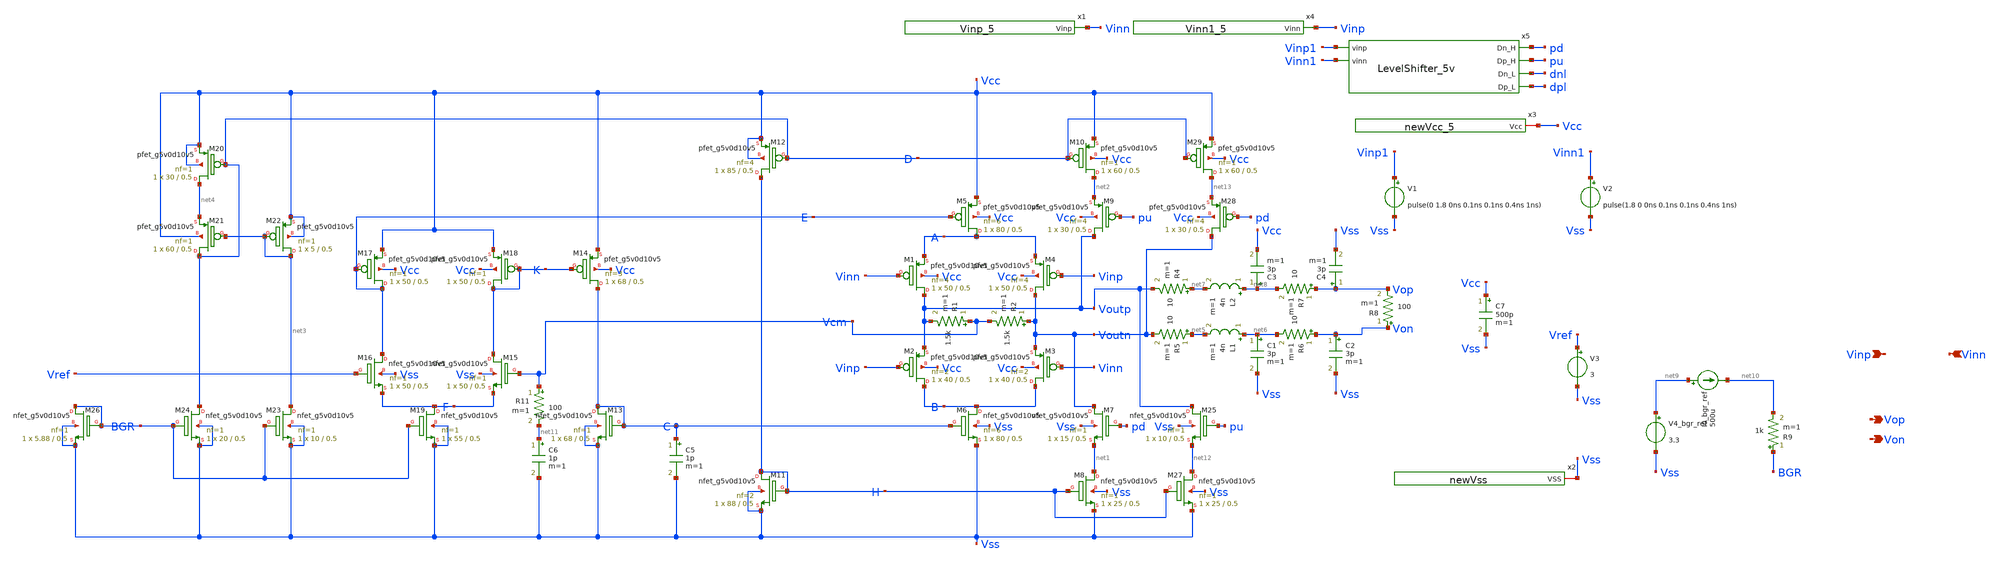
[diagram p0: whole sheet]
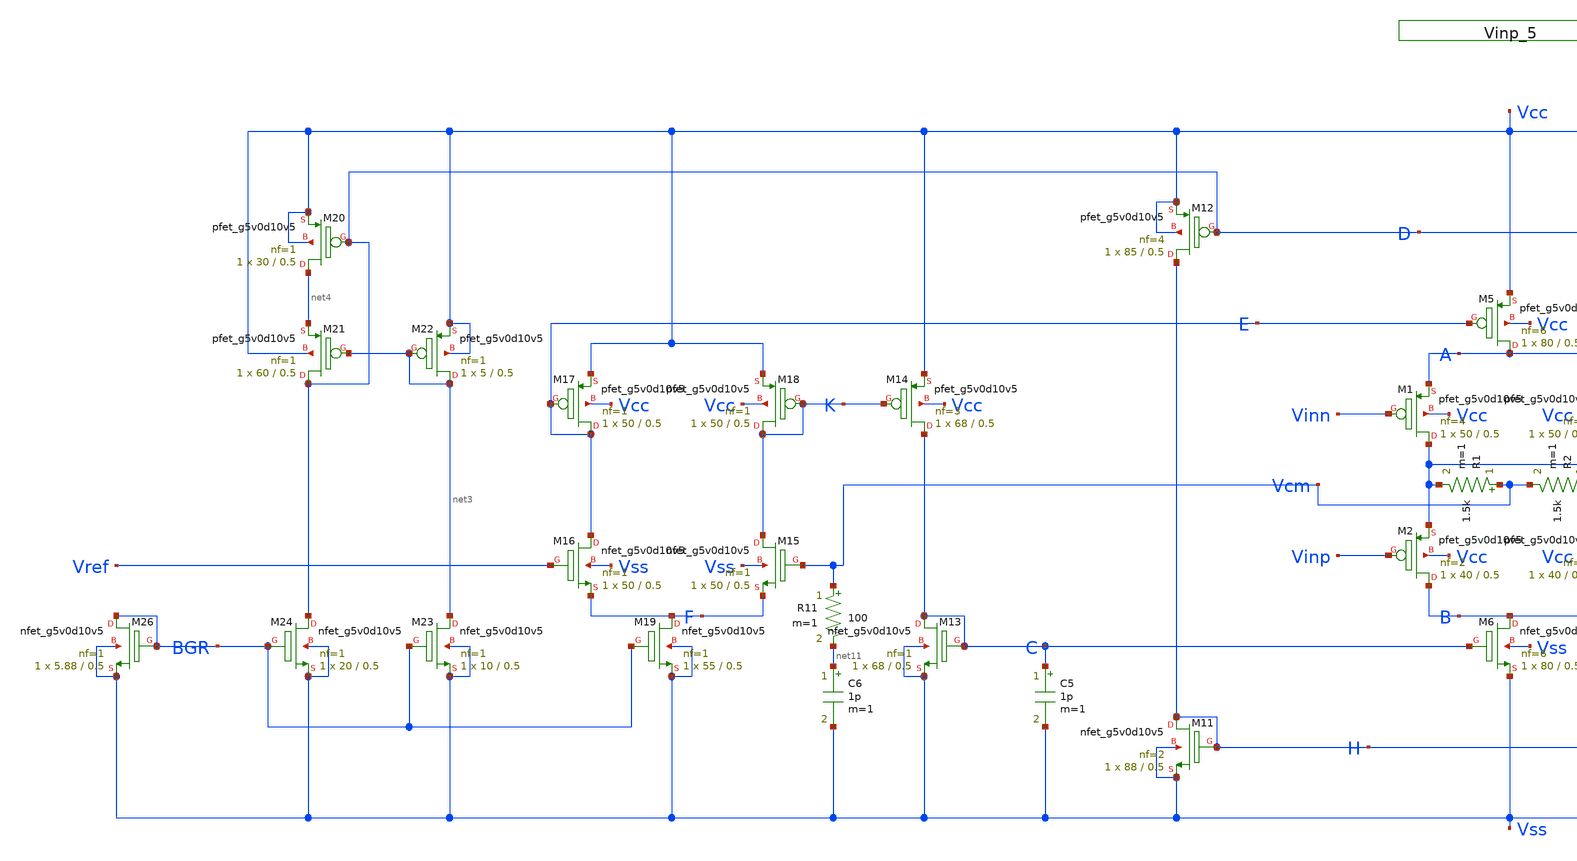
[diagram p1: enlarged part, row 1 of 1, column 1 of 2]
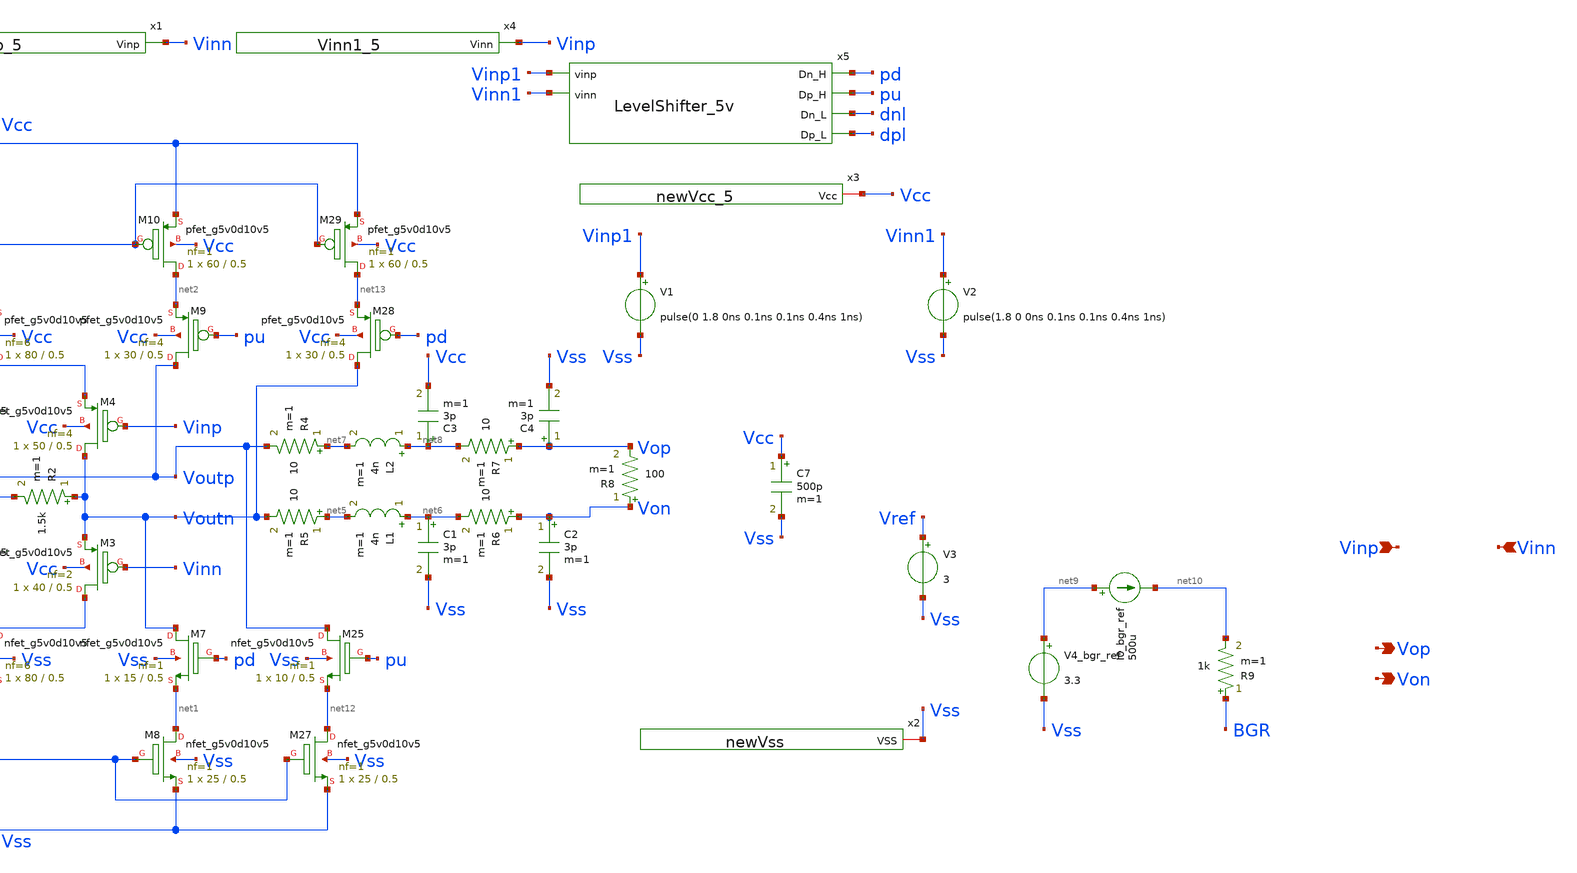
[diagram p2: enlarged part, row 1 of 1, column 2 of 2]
** sch_path: Git Files/Simulation Schematic/OutputDriverOffice_5v_sym.sch
**.subckt OutputDriverOffice_5v_sym Vinp Vinn Vop Von
*.ipin Vinp
*.ipin Vinn
*.opin Vop
*.opin Von
x2 Vss newVss
R1 Vcm Voutp 1.5k m=1
R2 Voutn Vcm 1.5k m=1
V3 Vref Vss 3
I0_bgr_ref net9 net10 500u
R4 net7 Voutp 10 m=1
R5 net5 Voutn 10 m=1
C1 net6 Vss 3p m=1
R6 Von net6 10 m=1
C2 Von Vss 3p m=1
C3 net8 Vcc 3p m=1
R7 Vop net8 10 m=1
C4 Vop Vss 3p m=1
R9 BGR net10 1k m=1
V4_bgr_ref net9 Vss 3.3
R8 Von Vop 100 m=1
C5 C Vss 1p m=1
C6 net11 Vss 1p m=1
L1 net6 net5 4n m=1
L2 net8 net7 4n m=1
R11 Vcm net11 100 m=1
C7 Vcc Vss 500p m=1
V1 Vinp1 Vss pulse(0 1.8 0ns 0.1ns 0.1ns 0.4ns 1ns)
V2 Vinn1 Vss pulse(1.8 0 0ns 0.1ns 0.1ns 0.4ns 1ns)
XM27 net12 H Vss Vss sky130_fd_pr__nfet_g5v0d10v5 L=0.5 W=25 nf=1 ad='int((nf+1)/2) * W/nf * 0.29' as='int((nf+2)/2) * W/nf * 0.29'
+ pd='2*int((nf+1)/2) * (W/nf + 0.29)' ps='2*int((nf+2)/2) * (W/nf + 0.29)' nrd='0.29 / W' nrs='0.29 / W'
+ sa=0 sb=0 sd=0 mult=1 m=1
XM8 net1 H Vss Vss sky130_fd_pr__nfet_g5v0d10v5 L=0.5 W=25 nf=1 ad='int((nf+1)/2) * W/nf * 0.29' as='int((nf+2)/2) * W/nf * 0.29'
+ pd='2*int((nf+1)/2) * (W/nf + 0.29)' ps='2*int((nf+2)/2) * (W/nf + 0.29)' nrd='0.29 / W' nrs='0.29 / W'
+ sa=0 sb=0 sd=0 mult=1 m=1
XM25 Voutp pu net12 Vss sky130_fd_pr__nfet_g5v0d10v5 L=0.5 W=10 nf=1 ad='int((nf+1)/2) * W/nf * 0.29'
+ as='int((nf+2)/2) * W/nf * 0.29' pd='2*int((nf+1)/2) * (W/nf + 0.29)' ps='2*int((nf+2)/2) * (W/nf + 0.29)'
+ nrd='0.29 / W' nrs='0.29 / W' sa=0 sb=0 sd=0 mult=1 m=1
XM7 Voutn pd net1 Vss sky130_fd_pr__nfet_g5v0d10v5 L=0.5 W=15 nf=1 ad='int((nf+1)/2) * W/nf * 0.29' as='int((nf+2)/2) * W/nf * 0.29'
+ pd='2*int((nf+1)/2) * (W/nf + 0.29)' ps='2*int((nf+2)/2) * (W/nf + 0.29)' nrd='0.29 / W' nrs='0.29 / W'
+ sa=0 sb=0 sd=0 mult=1 m=1
XM6 B C Vss Vss sky130_fd_pr__nfet_g5v0d10v5 L=0.5 W=80 nf=6 ad='int((nf+1)/2) * W/nf * 0.29' as='int((nf+2)/2) * W/nf * 0.29'
+ pd='2*int((nf+1)/2) * (W/nf + 0.29)' ps='2*int((nf+2)/2) * (W/nf + 0.29)' nrd='0.29 / W' nrs='0.29 / W'
+ sa=0 sb=0 sd=0 mult=1 m=1
XM11 H H Vss Vss sky130_fd_pr__nfet_g5v0d10v5 L=0.5 W=88 nf=2 ad='int((nf+1)/2) * W/nf * 0.29' as='int((nf+2)/2) * W/nf * 0.29'
+ pd='2*int((nf+1)/2) * (W/nf + 0.29)' ps='2*int((nf+2)/2) * (W/nf + 0.29)' nrd='0.29 / W' nrs='0.29 / W'
+ sa=0 sb=0 sd=0 mult=1 m=1
XM13 C C Vss Vss sky130_fd_pr__nfet_g5v0d10v5 L=0.5 W=68 nf=1 ad='int((nf+1)/2) * W/nf * 0.29' as='int((nf+2)/2) * W/nf * 0.29'
+ pd='2*int((nf+1)/2) * (W/nf + 0.29)' ps='2*int((nf+2)/2) * (W/nf + 0.29)' nrd='0.29 / W' nrs='0.29 / W'
+ sa=0 sb=0 sd=0 mult=1 m=1
XM15 K Vcm F Vss sky130_fd_pr__nfet_g5v0d10v5 L=0.5 W=50 nf=1 ad='int((nf+1)/2) * W/nf * 0.29' as='int((nf+2)/2) * W/nf * 0.29'
+ pd='2*int((nf+1)/2) * (W/nf + 0.29)' ps='2*int((nf+2)/2) * (W/nf + 0.29)' nrd='0.29 / W' nrs='0.29 / W'
+ sa=0 sb=0 sd=0 mult=1 m=1
XM19 F BGR Vss Vss sky130_fd_pr__nfet_g5v0d10v5 L=0.5 W=55 nf=1 ad='int((nf+1)/2) * W/nf * 0.29' as='int((nf+2)/2) * W/nf * 0.29'
+ pd='2*int((nf+1)/2) * (W/nf + 0.29)' ps='2*int((nf+2)/2) * (W/nf + 0.29)' nrd='0.29 / W' nrs='0.29 / W'
+ sa=0 sb=0 sd=0 mult=1 m=1
XM16 E Vref F Vss sky130_fd_pr__nfet_g5v0d10v5 L=0.5 W=50 nf=1 ad='int((nf+1)/2) * W/nf * 0.29' as='int((nf+2)/2) * W/nf * 0.29'
+ pd='2*int((nf+1)/2) * (W/nf + 0.29)' ps='2*int((nf+2)/2) * (W/nf + 0.29)' nrd='0.29 / W' nrs='0.29 / W'
+ sa=0 sb=0 sd=0 mult=1 m=1
XM23 net3 BGR Vss Vss sky130_fd_pr__nfet_g5v0d10v5 L=0.5 W=10 nf=1 ad='int((nf+1)/2) * W/nf * 0.29' as='int((nf+2)/2) * W/nf * 0.29'
+ pd='2*int((nf+1)/2) * (W/nf + 0.29)' ps='2*int((nf+2)/2) * (W/nf + 0.29)' nrd='0.29 / W' nrs='0.29 / W'
+ sa=0 sb=0 sd=0 mult=1 m=1
XM24 D BGR Vss Vss sky130_fd_pr__nfet_g5v0d10v5 L=0.5 W=20 nf=1 ad='int((nf+1)/2) * W/nf * 0.29' as='int((nf+2)/2) * W/nf * 0.29'
+ pd='2*int((nf+1)/2) * (W/nf + 0.29)' ps='2*int((nf+2)/2) * (W/nf + 0.29)' nrd='0.29 / W' nrs='0.29 / W'
+ sa=0 sb=0 sd=0 mult=1 m=1
XM26 BGR BGR Vss Vss sky130_fd_pr__nfet_g5v0d10v5 L=0.5 W=5.88 nf=1 ad='int((nf+1)/2) * W/nf * 0.29'
+ as='int((nf+2)/2) * W/nf * 0.29' pd='2*int((nf+1)/2) * (W/nf + 0.29)' ps='2*int((nf+2)/2) * (W/nf + 0.29)'
+ nrd='0.29 / W' nrs='0.29 / W' sa=0 sb=0 sd=0 mult=1 m=1
XM21 D net3 net4 Vcc sky130_fd_pr__pfet_g5v0d10v5 L=0.5 W=60 nf=1 ad='int((nf+1)/2) * W/nf * 0.29' as='int((nf+2)/2) * W/nf * 0.29'
+ pd='2*int((nf+1)/2) * (W/nf + 0.29)' ps='2*int((nf+2)/2) * (W/nf + 0.29)' nrd='0.29 / W' nrs='0.29 / W'
+ sa=0 sb=0 sd=0 mult=1 m=1
XM20 net4 D Vcc Vcc sky130_fd_pr__pfet_g5v0d10v5 L=0.5 W=30 nf=1 ad='int((nf+1)/2) * W/nf * 0.29' as='int((nf+2)/2) * W/nf * 0.29'
+ pd='2*int((nf+1)/2) * (W/nf + 0.29)' ps='2*int((nf+2)/2) * (W/nf + 0.29)' nrd='0.29 / W' nrs='0.29 / W'
+ sa=0 sb=0 sd=0 mult=1 m=1
XM22 net3 net3 Vcc Vcc sky130_fd_pr__pfet_g5v0d10v5 L=0.5 W=5 nf=1 ad='int((nf+1)/2) * W/nf * 0.29' as='int((nf+2)/2) * W/nf * 0.29'
+ pd='2*int((nf+1)/2) * (W/nf + 0.29)' ps='2*int((nf+2)/2) * (W/nf + 0.29)' nrd='0.29 / W' nrs='0.29 / W'
+ sa=0 sb=0 sd=0 mult=1 m=1
XM17 E E Vcc Vcc sky130_fd_pr__pfet_g5v0d10v5 L=0.5 W=50 nf=1 ad='int((nf+1)/2) * W/nf * 0.29' as='int((nf+2)/2) * W/nf * 0.29'
+ pd='2*int((nf+1)/2) * (W/nf + 0.29)' ps='2*int((nf+2)/2) * (W/nf + 0.29)' nrd='0.29 / W' nrs='0.29 / W'
+ sa=0 sb=0 sd=0 mult=1 m=1
XM18 K K Vcc Vcc sky130_fd_pr__pfet_g5v0d10v5 L=0.5 W=50 nf=1 ad='int((nf+1)/2) * W/nf * 0.29' as='int((nf+2)/2) * W/nf * 0.29'
+ pd='2*int((nf+1)/2) * (W/nf + 0.29)' ps='2*int((nf+2)/2) * (W/nf + 0.29)' nrd='0.29 / W' nrs='0.29 / W'
+ sa=0 sb=0 sd=0 mult=1 m=1
XM14 C K Vcc Vcc sky130_fd_pr__pfet_g5v0d10v5 L=0.5 W=68 nf=3 ad='int((nf+1)/2) * W/nf * 0.29' as='int((nf+2)/2) * W/nf * 0.29'
+ pd='2*int((nf+1)/2) * (W/nf + 0.29)' ps='2*int((nf+2)/2) * (W/nf + 0.29)' nrd='0.29 / W' nrs='0.29 / W'
+ sa=0 sb=0 sd=0 mult=1 m=1
XM12 H D Vcc Vcc sky130_fd_pr__pfet_g5v0d10v5 L=0.5 W=85 nf=4 ad='int((nf+1)/2) * W/nf * 0.29' as='int((nf+2)/2) * W/nf * 0.29'
+ pd='2*int((nf+1)/2) * (W/nf + 0.29)' ps='2*int((nf+2)/2) * (W/nf + 0.29)' nrd='0.29 / W' nrs='0.29 / W'
+ sa=0 sb=0 sd=0 mult=1 m=1
XM1 Voutp Vinn A Vcc sky130_fd_pr__pfet_g5v0d10v5 L=0.5 W=50 nf=4 ad='int((nf+1)/2) * W/nf * 0.29' as='int((nf+2)/2) * W/nf * 0.29'
+ pd='2*int((nf+1)/2) * (W/nf + 0.29)' ps='2*int((nf+2)/2) * (W/nf + 0.29)' nrd='0.29 / W' nrs='0.29 / W'
+ sa=0 sb=0 sd=0 mult=1 m=1
XM4 Voutn Vinp A Vcc sky130_fd_pr__pfet_g5v0d10v5 L=0.5 W=50 nf=4 ad='int((nf+1)/2) * W/nf * 0.29' as='int((nf+2)/2) * W/nf * 0.29'
+ pd='2*int((nf+1)/2) * (W/nf + 0.29)' ps='2*int((nf+2)/2) * (W/nf + 0.29)' nrd='0.29 / W' nrs='0.29 / W'
+ sa=0 sb=0 sd=0 mult=1 m=1
XM3 B Vinn Voutn Vcc sky130_fd_pr__pfet_g5v0d10v5 L=0.5 W=40 nf=2 ad='int((nf+1)/2) * W/nf * 0.29' as='int((nf+2)/2) * W/nf * 0.29'
+ pd='2*int((nf+1)/2) * (W/nf + 0.29)' ps='2*int((nf+2)/2) * (W/nf + 0.29)' nrd='0.29 / W' nrs='0.29 / W'
+ sa=0 sb=0 sd=0 mult=1 m=1
XM2 B Vinp Voutp Vcc sky130_fd_pr__pfet_g5v0d10v5 L=0.5 W=40 nf=2 ad='int((nf+1)/2) * W/nf * 0.29' as='int((nf+2)/2) * W/nf * 0.29'
+ pd='2*int((nf+1)/2) * (W/nf + 0.29)' ps='2*int((nf+2)/2) * (W/nf + 0.29)' nrd='0.29 / W' nrs='0.29 / W'
+ sa=0 sb=0 sd=0 mult=1 m=1
XM5 A E Vcc Vcc sky130_fd_pr__pfet_g5v0d10v5 L=0.5 W=80 nf=6 ad='int((nf+1)/2) * W/nf * 0.29' as='int((nf+2)/2) * W/nf * 0.29'
+ pd='2*int((nf+1)/2) * (W/nf + 0.29)' ps='2*int((nf+2)/2) * (W/nf + 0.29)' nrd='0.29 / W' nrs='0.29 / W'
+ sa=0 sb=0 sd=0 mult=1 m=1
XM10 net2 D Vcc Vcc sky130_fd_pr__pfet_g5v0d10v5 L=0.5 W=60 nf=1 ad='int((nf+1)/2) * W/nf * 0.29' as='int((nf+2)/2) * W/nf * 0.29'
+ pd='2*int((nf+1)/2) * (W/nf + 0.29)' ps='2*int((nf+2)/2) * (W/nf + 0.29)' nrd='0.29 / W' nrs='0.29 / W'
+ sa=0 sb=0 sd=0 mult=1 m=1
XM9 Voutp pu net2 Vcc sky130_fd_pr__pfet_g5v0d10v5 L=0.5 W=30 nf=4 ad='int((nf+1)/2) * W/nf * 0.29' as='int((nf+2)/2) * W/nf * 0.29'
+ pd='2*int((nf+1)/2) * (W/nf + 0.29)' ps='2*int((nf+2)/2) * (W/nf + 0.29)' nrd='0.29 / W' nrs='0.29 / W'
+ sa=0 sb=0 sd=0 mult=1 m=1
XM28 Voutn pd net13 Vcc sky130_fd_pr__pfet_g5v0d10v5 L=0.5 W=30 nf=4 ad='int((nf+1)/2) * W/nf * 0.29'
+ as='int((nf+2)/2) * W/nf * 0.29' pd='2*int((nf+1)/2) * (W/nf + 0.29)' ps='2*int((nf+2)/2) * (W/nf + 0.29)'
+ nrd='0.29 / W' nrs='0.29 / W' sa=0 sb=0 sd=0 mult=1 m=1
XM29 net13 D Vcc Vcc sky130_fd_pr__pfet_g5v0d10v5 L=0.5 W=60 nf=1 ad='int((nf+1)/2) * W/nf * 0.29' as='int((nf+2)/2) * W/nf * 0.29'
+ pd='2*int((nf+1)/2) * (W/nf + 0.29)' ps='2*int((nf+2)/2) * (W/nf + 0.29)' nrd='0.29 / W' nrs='0.29 / W'
+ sa=0 sb=0 sd=0 mult=1 m=1
x5 pd pu Vinp1 Vinn1 dnl dpl LevelShifter_5v
x3 Vcc newVcc_5
x1 Vinn Vinp_5
x4 Vinp Vinn1_5
**.ends
.end
